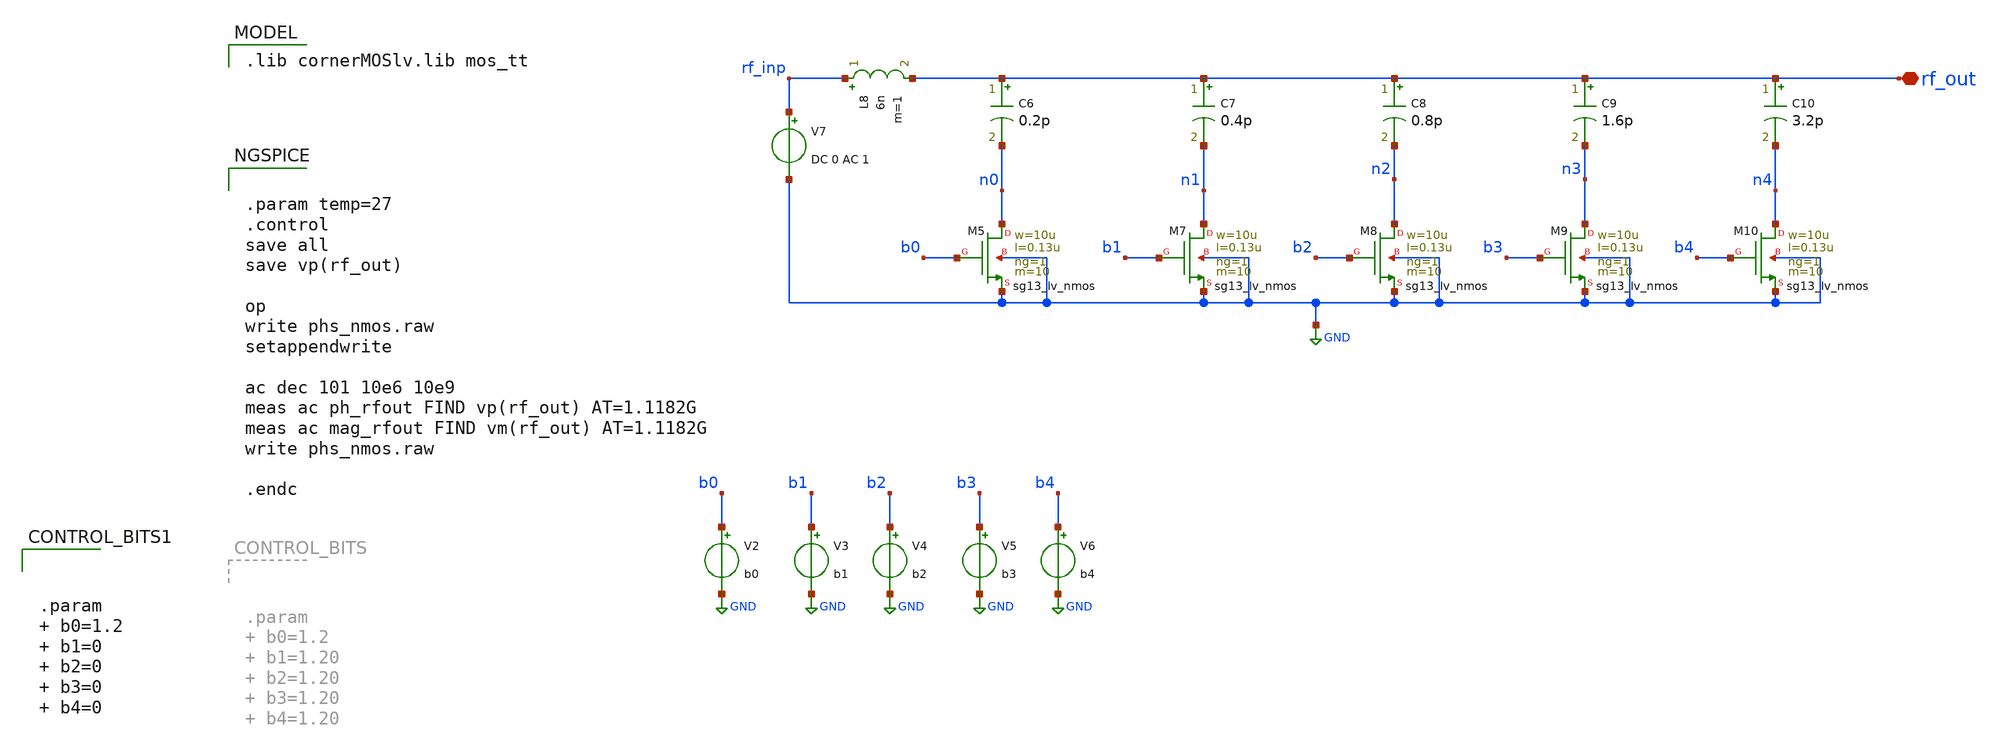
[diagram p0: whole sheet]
** sch_path: xschem/phs_nmos.sch
**.subckt phs_nmos rf_out
*.iopin rf_out
V2 b0 GND b0
V3 b1 GND b1
V4 b2 GND b2
V5 b3 GND b3
V6 b4 GND b4
L8 rf_inp rf_out 6n m=1
C6 rf_out n0 0.2p m=1
C7 rf_out n1 0.4p m=1
C8 rf_out n2 0.8p m=1
C9 rf_out n3 1.6p m=1
C10 rf_out n4 3.2p m=1
V7 rf_inp GND DC 0 AC 1
XM5 n0 b0 GND GND sg13_lv_nmos w=10u l=0.13u ng=1 m=10 mm_ok=1
XM7 n1 b1 GND GND sg13_lv_nmos w=10u l=0.13u ng=1 m=10 mm_ok=1
XM8 n2 b2 GND GND sg13_lv_nmos w=10u l=0.13u ng=1 m=10 mm_ok=1
XM9 n3 b3 GND GND sg13_lv_nmos w=10u l=0.13u ng=1 m=10 mm_ok=1
XM10 n4 b4 GND GND sg13_lv_nmos w=10u l=0.13u ng=1 m=10 mm_ok=1
**** begin user architecture code
 .lib cornerMOSlv.lib mos_tt



.param temp=27
.control
save all
save vp(rf_out)

op
write phs_nmos.raw
setappendwrite

ac dec 101 10e6 10e9
meas ac ph_rfout FIND vp(rf_out) AT=1.1182G
meas ac mag_rfout FIND vm(rf_out) AT=1.1182G
write phs_nmos.raw

.endc





.param   b0=1.2  b1=0  b2=0  b3=0  b4=0


**** end user architecture code
**.ends
.GLOBAL GND
.end
